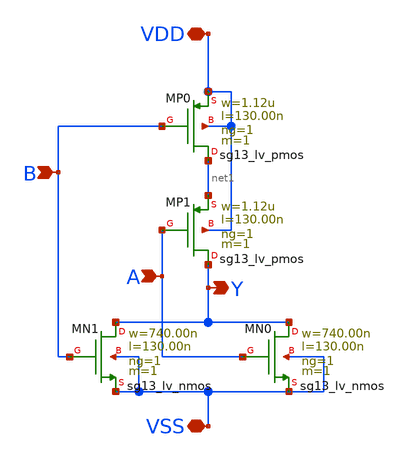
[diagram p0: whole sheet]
** sch_path: netlist/NOR.sch
**.subckt NOR Y A VDD VSS B
*.opin Y
*.ipin A
*.iopin VDD
*.iopin VSS
*.ipin B
XMN0 Y A VSS VSS sg13_lv_nmos w=740.00n l=130.00n ng=1 m=1 mm_ok=1
XMP0 net1 B VDD VDD sg13_lv_pmos w=1.12u l=130.00n ng=1 m=1 mm_ok=1
XMP1 Y A net1 VDD sg13_lv_pmos w=1.12u l=130.00n ng=1 m=1 mm_ok=1
XMN1 Y B VSS VSS sg13_lv_nmos w=740.00n l=130.00n ng=1 m=1 mm_ok=1
**.ends
.end
